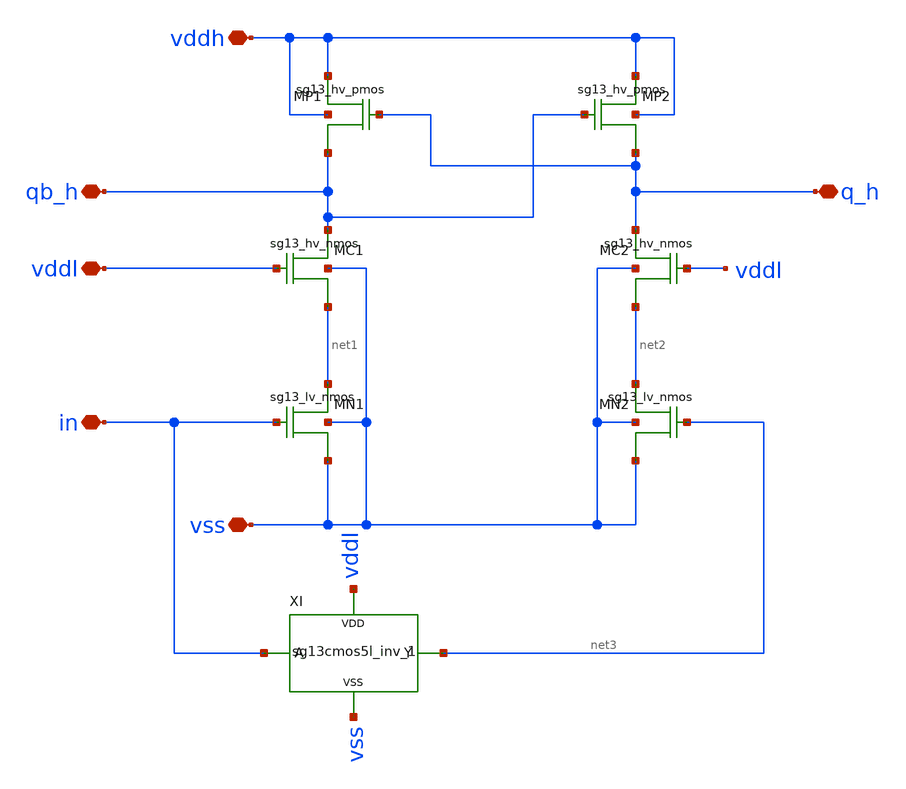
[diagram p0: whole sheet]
** sch_path: xschem/schematics/level_shifter_up.sch
**.subckt level_shifter_up vddh vss qb_h q_h vddl in
*.iopin vddh
*.iopin vss
*.iopin qb_h
*.iopin q_h
*.iopin vddl
*.iopin in
XMP1 vddh q_h qb_h vddh sg13_hv_pmos w=0.5u l=1.6u ng=1 m=1
XMP2 vddh qb_h q_h vddh sg13_hv_pmos w=0.5u l=1.6u ng=1 m=1
XMC1 qb_h vddl net1 vss sg13_hv_nmos w=1.5u l=0.45u ng=1 m=1
XMC2 q_h vddl net2 vss sg13_hv_nmos w=1.5u l=0.45u ng=1 m=1
XMN1 net1 in vss vss sg13_lv_nmos w=1.0u l=0.13u ng=1 m=1
XMN2 net2 net3 vss vss sg13_lv_nmos w=1.0u l=0.13u ng=1 m=1
XI net3 in vddl vss sg13cmos5l_inv_1
**.ends

* expanding   symbol:  logic_gates/sg13cmos5l_inv_1.sym # of pins=4
** sym_path: xschem/logic_gates/sg13cmos5l_inv_1.sym
** sch_path: xschem/logic_gates/sg13cmos5l_inv_1.sch
.subckt sg13cmos5l_inv_1 Y A VDD VSS
*.iopin Y
*.iopin A
*.iopin VDD
*.iopin VSS
XMN0 Y A VSS VSS sg13_lv_nmos w=0.74u l=0.13u ng=1 m=1
XMP0 VDD A Y VDD sg13_lv_pmos w=1.12u l=0.13u ng=1 m=1
.ends

.end
